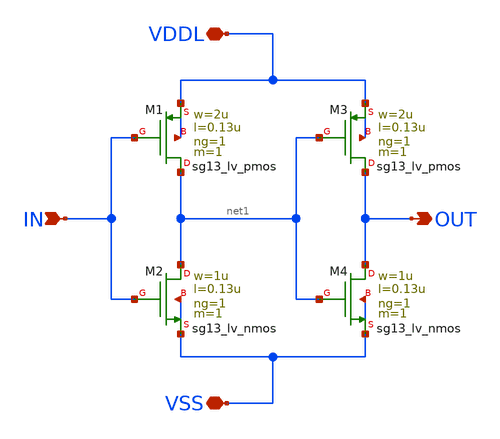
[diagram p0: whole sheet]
** sch_path: SSDOR_1.2V_v3/components/logic_shift_down_v1/logic_shift_down_v1.sch
**.subckt logic_shift_down_v1 IN OUT VDDL VSS
*.ipin IN
*.opin OUT
*.iopin VDDL
*.iopin VSS
XM1 net1 IN VDDL VDDL sg13_lv_pmos w=2u l=0.13u ng=1 m=1 mm_ok=1
XM2 net1 IN VSS VSS sg13_lv_nmos w=1u l=0.13u ng=1 m=1 mm_ok=1
XM3 OUT net1 VDDL VDDL sg13_lv_pmos w=2u l=0.13u ng=1 m=1 mm_ok=1
XM4 OUT net1 VSS VSS sg13_lv_nmos w=1u l=0.13u ng=1 m=1 mm_ok=1
**.ends
.end
